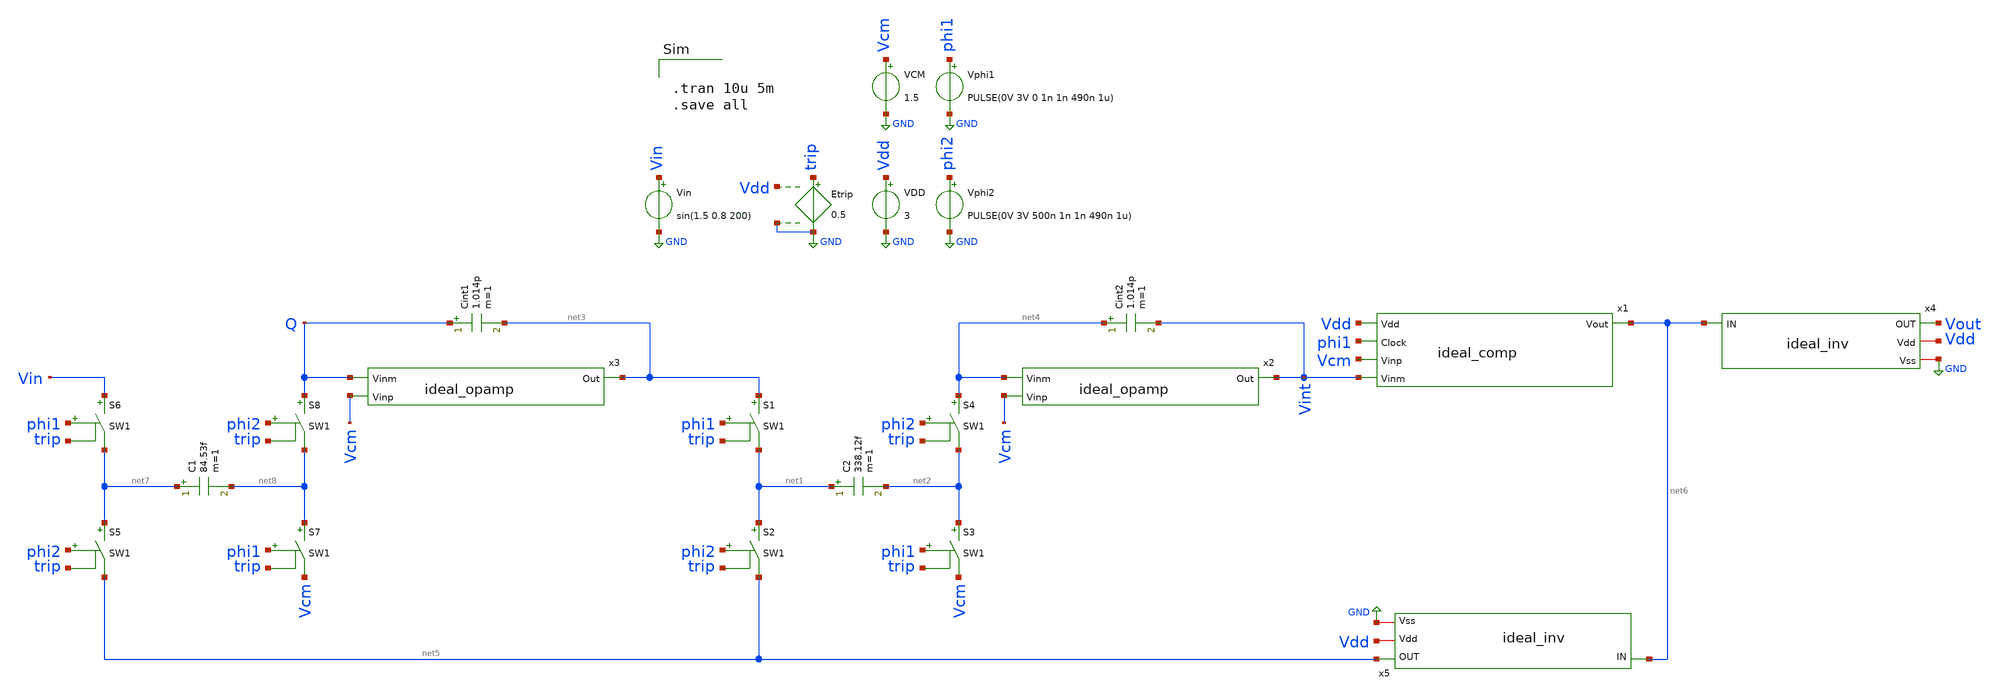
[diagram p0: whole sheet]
** sch_path: ideal_circuit/xschem/ideal_circuit.sch
**.subckt ideal_circuit
Etrip trip GND Vdd GND 0.5
VDD Vdd GND 3
VCM Vcm GND 1.5
Vin Vin GND sin(1.5 0.8 200)
Vphi1 phi1 GND PULSE(0V 3V 0 1n 1n 490n 1u)
Vphi2 phi2 GND PULSE(0V 3V 500n 1n 1n 490n 1u)
C2 net1 net2 338.12f m=1
S2 net1 net5 phi2 trip SW1
S1 net3 net1 phi1 trip SW1
S3 net2 Vcm phi1 trip SW1
S4 net4 net2 phi2 trip SW1
Cint2 net4 Vint 1.014p m=1
C1 net7 net8 84.53f m=1
S5 net7 net5 phi2 trip SW1
S6 Vin net7 phi1 trip SW1
S7 net8 Vcm phi1 trip SW1
S8 Q net8 phi2 trip SW1
Cint1 Q net3 1.014p m=1
x1 net6 Vdd phi1 Vcm Vint ideal_comp
x2 Vint net4 Vcm ideal_opamp
x3 net3 Q Vcm ideal_opamp
x4 Vout Vdd net6 GND ideal_inv
x5 net5 Vdd net6 GND ideal_inv
**** begin user architecture code


.tran 10u 5m
.save all


**** end user architecture code
**.ends
.GLOBAL GND
**** begin user architecture code
.MODEL SW1 SW   VT=0.9 VH=0.01  RON=0.1 ROFF=10G
**** end user architecture code
.end
